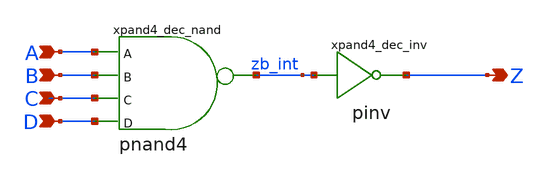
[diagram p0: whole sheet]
** sch_path: sram_2_64_scn4m_lcc/and4_dec.sch
**.subckt and4_dec A B C D Z
*.ipin A
*.ipin B
*.ipin C
*.ipin D
*.opin Z
xpand4_dec_nand A B C D zb_int vdd gnd pnand4
xpand4_dec_inv zb_int Z vdd gnd pinv
**.ends
.end
